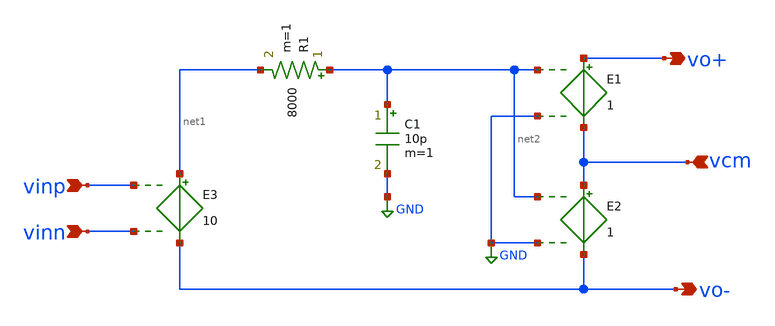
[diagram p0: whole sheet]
** sch_path: XSCHEM/XSCHEM files/diff_opamp.sch
**.subckt diff_opamp vinp vo- vinn vo+ vcm
*.ipin vinp
*.opin vo-
*.ipin vinn
*.opin vo+
*.ipin vcm
E1 vo+ vcm net2 GND 1
E3 net1 vo- vinp vinn 10
R1 net2 net1 8000 m=1
C1 net2 GND 10p m=1
E2 vcm vo- net2 GND 1
**.ends
.GLOBAL GND
.end
